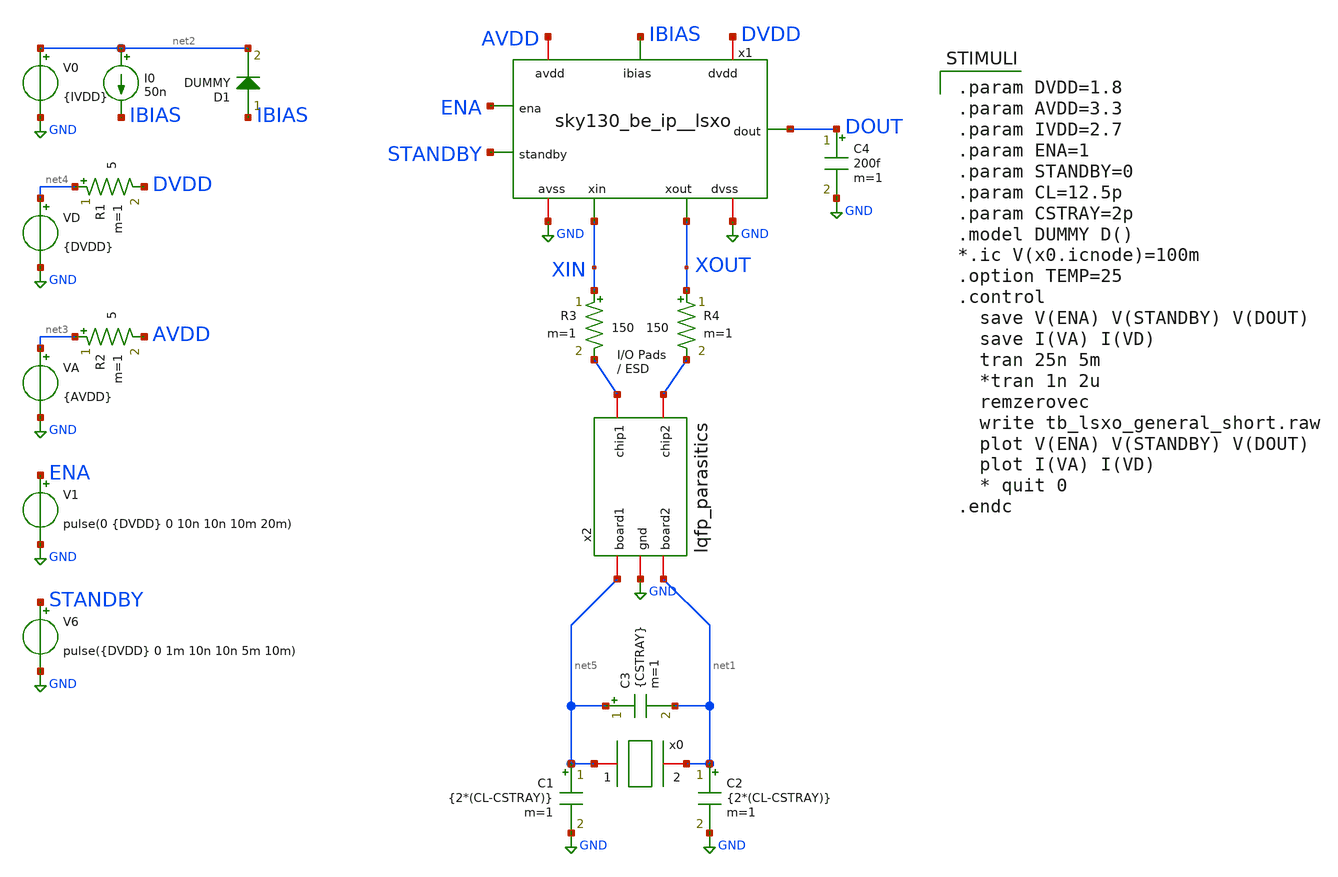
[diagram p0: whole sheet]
** sch_path: xschem/tb_sky130_be_ip__lsxo.sch

.lib $::SKYWATER_MODELS/sky130.lib.spice ff
.include $::SKYWATER_STDCELLS/sky130_fd_sc_hd.spice

**.subckt tb_sky130_be_ip__lsxo
VD net4 GND {DVDD}
VA net3 GND {AVDD}
C1 net5 GND {2*(CL-CSTRAY)} m=1
C2 net1 GND {2*(CL-CSTRAY)} m=1
C3 net5 net1 {CSTRAY} m=1
I0 net2 IBIAS 50n
C4 DOUT GND 200f m=1
V0 net2 GND {IVDD}
V6 STANDBY GND pulse({DVDD} 0 1m 10n 10n 5m 10m)
R1 net4 DVDD 5 m=1
R2 net3 AVDD 5 m=1
R3 XIN net6 150 m=1
R4 XOUT net7 150 m=1
x2 net7 net6 GND net5 net1 lqfp_parasitics
V1 ENA GND pulse(0 {DVDD} 0 10n 10n 10m 20m)
D1 IBIAS net2 DUMMY area=100
x1 AVDD GND DVDD GND IBIAS ENA STANDBY DOUT XIN XOUT sky130_be_ip__lsxo
x0 net5 net1 xtal_iqd_125_1
**** begin user architecture code

.param DVDD=1.8
.param AVDD=3.3
.param IVDD=2.7
.param ENA=1
.param STANDBY=0
.param CL=12.5p
.param CSTRAY=2p
.model DUMMY D()
*.ic V(x0.icnode)=100m
.option TEMP=25
.control
  save V(ENA) V(STANDBY) V(DOUT)
  save I(VA) I(VD)
  tran 25n 5m
  *tran 1n 2u
  remzerovec
  write tb_lsxo_general_short.raw
  plot V(ENA) V(STANDBY) V(DOUT)
  plot I(VA) I(VD)
  * quit 0
.endc

**** end user architecture code
**.ends
.GLOBAL GND
.end
